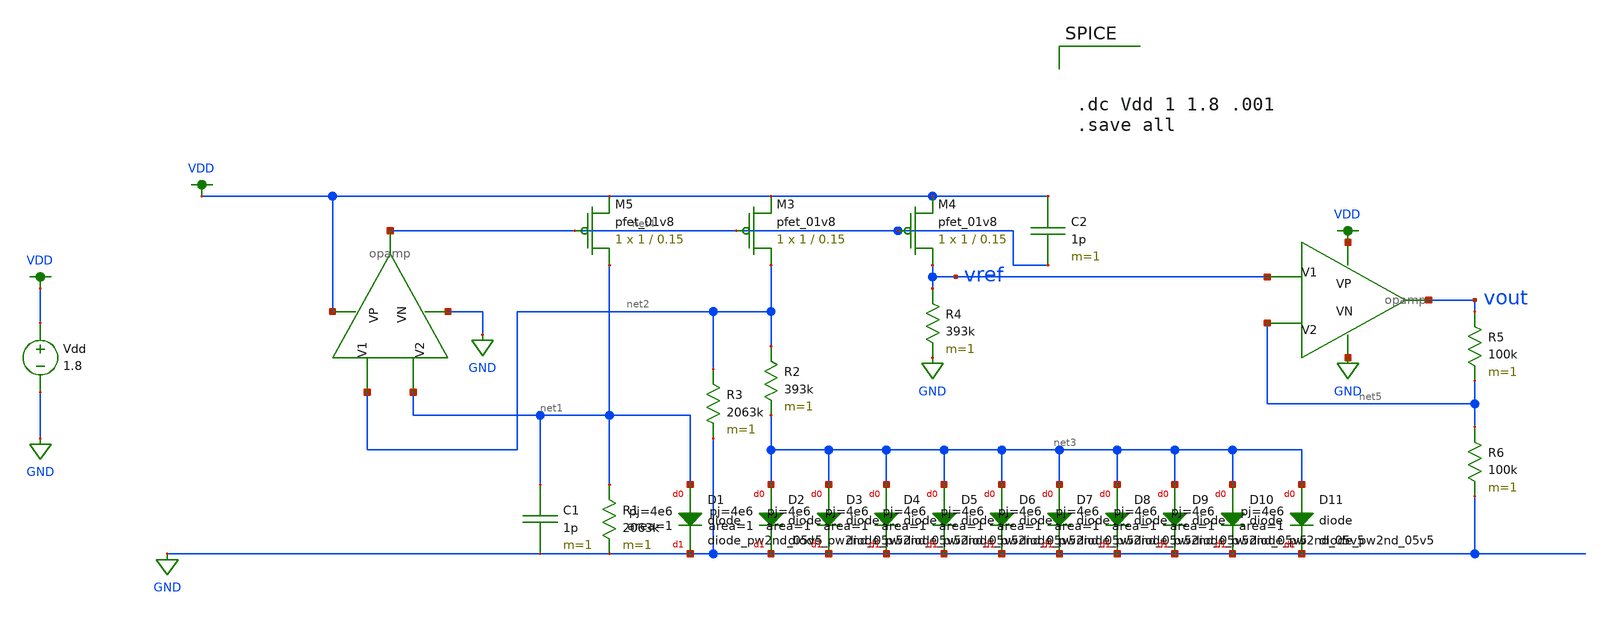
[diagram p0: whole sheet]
** sch_path: schematics/bandgap.sch
**.subckt bandgap
XD1 net1 GND sky130_fd_pr__diode_pw2nd_05v5 area=1 pj=4e6
XM4 vref net4 VDD VDD sky130_fd_pr__pfet_01v8 L=0.15 W=1 nf=1 ad='int((nf+1)/2) * W/nf * 0.29' as='int((nf+2)/2) * W/nf * 0.29'
+ pd='2*int((nf+1)/2) * (W/nf + 0.29)' ps='2*int((nf+2)/2) * (W/nf + 0.29)' nrd='0.29 / W' nrs='0.29 / W'
+ sa=0 sb=0 sd=0 mult=1 m=1
XM5 net1 net4 VDD VDD sky130_fd_pr__pfet_01v8 L=0.15 W=1 nf=1 ad='int((nf+1)/2) * W/nf * 0.29' as='int((nf+2)/2) * W/nf * 0.29'
+ pd='2*int((nf+1)/2) * (W/nf + 0.29)' ps='2*int((nf+2)/2) * (W/nf + 0.29)' nrd='0.29 / W' nrs='0.29 / W'
+ sa=0 sb=0 sd=0 mult=1 m=1
XM3 net2 net4 VDD VDD sky130_fd_pr__pfet_01v8 L=0.15 W=1 nf=1 ad='int((nf+1)/2) * W/nf * 0.29' as='int((nf+2)/2) * W/nf * 0.29'
+ pd='2*int((nf+1)/2) * (W/nf + 0.29)' ps='2*int((nf+2)/2) * (W/nf + 0.29)' nrd='0.29 / W' nrs='0.29 / W'
+ sa=0 sb=0 sd=0 mult=1 m=1
C1 net1 GND 1p m=1
R1 net1 GND 2063k m=1
XD2 net3 GND sky130_fd_pr__diode_pw2nd_05v5 area=1 pj=4e6
R2 net2 net3 393k m=1
XD3 net3 GND sky130_fd_pr__diode_pw2nd_05v5 area=1 pj=4e6
R3 net2 GND 2063k m=1
R4 vref GND 393k m=1
XD4 net3 GND sky130_fd_pr__diode_pw2nd_05v5 area=1 pj=4e6
XD5 net3 GND sky130_fd_pr__diode_pw2nd_05v5 area=1 pj=4e6
XD6 net3 GND sky130_fd_pr__diode_pw2nd_05v5 area=1 pj=4e6
XD7 net3 GND sky130_fd_pr__diode_pw2nd_05v5 area=1 pj=4e6
XD8 net3 GND sky130_fd_pr__diode_pw2nd_05v5 area=1 pj=4e6
XD9 net3 GND sky130_fd_pr__diode_pw2nd_05v5 area=1 pj=4e6
XD10 net3 GND sky130_fd_pr__diode_pw2nd_05v5 area=1 pj=4e6
XD11 net3 GND sky130_fd_pr__diode_pw2nd_05v5 area=1 pj=4e6
C2 VDD net4 1p m=1
Vdd VDD GND 1.8
X1 net2 net1 VDD GND net4 opamp
X2 vref net5 VDD GND vout opamp
R5 vout net5 100k m=1
R6 net5 GND 100k m=1
**** begin user architecture code

.option wnflag=1
.param MC_SWITCH=0.0
.lib ~/skywater/skywater-pdk/libraries/sky130_fd_pr_ngspice/latest/models/sky130.lib.spice tt




.dc Vdd 1 1.8 .001
.save all


**** end user architecture code
**.ends

* expanding   symbol:  /home/madvlsi/Documents/MADVLSI_final/schematics/opamp.sym # of pins=5
** sym_path: schematics/opamp.sym
** sch_path: schematics/opamp.sch
.subckt opamp V1 V2 VP VN Vout
*.ipin V1
*.ipin V2
*.opin Vout
*.iopin VP
*.iopin VN
*.iopin VP
*.iopin VN
XM1 VN net7 net2 GND sky130_fd_pr__nfet_01v8 L=l W=w nf=1 ad='int((nf+1)/2) * W/nf * 0.29' as='int((nf+2)/2) * W/nf * 0.29'
+ pd='2*int((nf+1)/2) * (W/nf + 0.29)' ps='2*int((nf+2)/2) * (W/nf + 0.29)' nrd='0.29 / W' nrs='0.29 / W'
+ sa=0 sb=0 sd=0 mult=1 m=1
XM2 VP net3 net1 VDD sky130_fd_pr__pfet_01v8 L=l W=w nf=1 ad='int((nf+1)/2) * W/nf * 0.29' as='int((nf+2)/2) * W/nf * 0.29'
+ pd='2*int((nf+1)/2) * (W/nf + 0.29)' ps='2*int((nf+2)/2) * (W/nf + 0.29)' nrd='0.29 / W' nrs='0.29 / W'
+ sa=0 sb=0 sd=0 mult=1 m=1
XM3 net1 V1 Vd VDD sky130_fd_pr__pfet_01v8 L=l W=w nf=1 ad='int((nf+1)/2) * W/nf * 0.29' as='int((nf+2)/2) * W/nf * 0.29'
+ pd='2*int((nf+1)/2) * (W/nf + 0.29)' ps='2*int((nf+2)/2) * (W/nf + 0.29)' nrd='0.29 / W' nrs='0.29 / W'
+ sa=0 sb=0 sd=0 mult=1 m=1
XM4 Vc V2 net1 VDD sky130_fd_pr__pfet_01v8 L=l W=w nf=1 ad='int((nf+1)/2) * W/nf * 0.29' as='int((nf+2)/2) * W/nf * 0.29'
+ pd='2*int((nf+1)/2) * (W/nf + 0.29)' ps='2*int((nf+2)/2) * (W/nf + 0.29)' nrd='0.29 / W' nrs='0.29 / W'
+ sa=0 sb=0 sd=0 mult=1 m=1
XM5 Va V2 net2 GND sky130_fd_pr__nfet_01v8 L=l W=w nf=1 ad='int((nf+1)/2) * W/nf * 0.29' as='int((nf+2)/2) * W/nf * 0.29'
+ pd='2*int((nf+1)/2) * (W/nf + 0.29)' ps='2*int((nf+2)/2) * (W/nf + 0.29)' nrd='0.29 / W' nrs='0.29 / W'
+ sa=0 sb=0 sd=0 mult=1 m=1
XM6 net2 V1 Vb GND sky130_fd_pr__nfet_01v8 L=l W=w nf=1 ad='int((nf+1)/2) * W/nf * 0.29' as='int((nf+2)/2) * W/nf * 0.29'
+ pd='2*int((nf+1)/2) * (W/nf + 0.29)' ps='2*int((nf+2)/2) * (W/nf + 0.29)' nrd='0.29 / W' nrs='0.29 / W'
+ sa=0 sb=0 sd=0 mult=1 m=1
XM7 net3 net3 Va VDD sky130_fd_pr__pfet_01v8 L=l W=w nf=1 ad='int((nf+1)/2) * W/nf * 0.29' as='int((nf+2)/2) * W/nf * 0.29'
+ pd='2*int((nf+1)/2) * (W/nf + 0.29)' ps='2*int((nf+2)/2) * (W/nf + 0.29)' nrd='0.29 / W' nrs='0.29 / W'
+ sa=0 sb=0 sd=0 mult=1 m=1
XM8 net6 net6 Va VDD sky130_fd_pr__pfet_01v8 L=l W=w nf=1 ad='int((nf+1)/2) * W/nf * 0.29' as='int((nf+2)/2) * W/nf * 0.29'
+ pd='2*int((nf+1)/2) * (W/nf + 0.29)' ps='2*int((nf+2)/2) * (W/nf + 0.29)' nrd='0.29 / W' nrs='0.29 / W'
+ sa=0 sb=0 sd=0 mult=1 m=1
XM9 net5 net6 Vb VDD sky130_fd_pr__pfet_01v8 L=l W=w nf=1 ad='int((nf+1)/2) * W/nf * 0.29' as='int((nf+2)/2) * W/nf * 0.29'
+ pd='2*int((nf+1)/2) * (W/nf + 0.29)' ps='2*int((nf+2)/2) * (W/nf + 0.29)' nrd='0.29 / W' nrs='0.29 / W'
+ sa=0 sb=0 sd=0 mult=1 m=1
XM10 Va net3 VP VDD sky130_fd_pr__pfet_01v8 L=l W=w nf=1 ad='int((nf+1)/2) * W/nf * 0.29' as='int((nf+2)/2) * W/nf * 0.29'
+ pd='2*int((nf+1)/2) * (W/nf + 0.29)' ps='2*int((nf+2)/2) * (W/nf + 0.29)' nrd='0.29 / W' nrs='0.29 / W'
+ sa=0 sb=0 sd=0 mult=1 m=1
XM11 Vb net3 VP VDD sky130_fd_pr__pfet_01v8 L=l W=w nf=1 ad='int((nf+1)/2) * W/nf * 0.29' as='int((nf+2)/2) * W/nf * 0.29'
+ pd='2*int((nf+1)/2) * (W/nf + 0.29)' ps='2*int((nf+2)/2) * (W/nf + 0.29)' nrd='0.29 / W' nrs='0.29 / W'
+ sa=0 sb=0 sd=0 mult=1 m=1
XM12 net6 net6 Vc GND sky130_fd_pr__nfet_01v8 L=l W=w nf=1 ad='int((nf+1)/2) * W/nf * 0.29' as='int((nf+2)/2) * W/nf * 0.29'
+ pd='2*int((nf+1)/2) * (W/nf + 0.29)' ps='2*int((nf+2)/2) * (W/nf + 0.29)' nrd='0.29 / W' nrs='0.29 / W'
+ sa=0 sb=0 sd=0 mult=1 m=1
XM13 net5 net6 Vd GND sky130_fd_pr__nfet_01v8 L=l W=w nf=1 ad='int((nf+1)/2) * W/nf * 0.29' as='int((nf+2)/2) * W/nf * 0.29'
+ pd='2*int((nf+1)/2) * (W/nf + 0.29)' ps='2*int((nf+2)/2) * (W/nf + 0.29)' nrd='0.29 / W' nrs='0.29 / W'
+ sa=0 sb=0 sd=0 mult=1 m=1
XM14 Vc net7 VN GND sky130_fd_pr__nfet_01v8 L=l W=w nf=1 ad='int((nf+1)/2) * W/nf * 0.29' as='int((nf+2)/2) * W/nf * 0.29'
+ pd='2*int((nf+1)/2) * (W/nf + 0.29)' ps='2*int((nf+2)/2) * (W/nf + 0.29)' nrd='0.29 / W' nrs='0.29 / W'
+ sa=0 sb=0 sd=0 mult=1 m=1
XM15 Vd net7 VN GND sky130_fd_pr__nfet_01v8 L=l W=w nf=1 ad='int((nf+1)/2) * W/nf * 0.29' as='int((nf+2)/2) * W/nf * 0.29'
+ pd='2*int((nf+1)/2) * (W/nf + 0.29)' ps='2*int((nf+2)/2) * (W/nf + 0.29)' nrd='0.29 / W' nrs='0.29 / W'
+ sa=0 sb=0 sd=0 mult=1 m=1
XM16 net8 net7 net3 GND sky130_fd_pr__nfet_01v8 L=l W=w nf=1 ad='int((nf+1)/2) * W/nf * 0.29' as='int((nf+2)/2) * W/nf * 0.29'
+ pd='2*int((nf+1)/2) * (W/nf + 0.29)' ps='2*int((nf+2)/2) * (W/nf + 0.29)' nrd='0.29 / W' nrs='0.29 / W'
+ sa=0 sb=0 sd=0 mult=1 m=1
XM17 VN net7 net8 GND sky130_fd_pr__nfet_01v8 L=l W=w nf=1 ad='int((nf+1)/2) * W/nf * 0.29' as='int((nf+2)/2) * W/nf * 0.29'
+ pd='2*int((nf+1)/2) * (W/nf + 0.29)' ps='2*int((nf+2)/2) * (W/nf + 0.29)' nrd='0.29 / W' nrs='0.29 / W'
+ sa=0 sb=0 sd=0 mult=1 m=1
XM18 net8 net7 VP GND sky130_fd_pr__nfet_01v8 L=l W=w nf=1 ad='int((nf+1)/2) * W/nf * 0.29' as='int((nf+2)/2) * W/nf * 0.29'
+ pd='2*int((nf+1)/2) * (W/nf + 0.29)' ps='2*int((nf+2)/2) * (W/nf + 0.29)' nrd='0.29 / W' nrs='0.29 / W'
+ sa=0 sb=0 sd=0 mult=M m=M
XM19 net4 net3 net7 VDD sky130_fd_pr__pfet_01v8 L=l W=w nf=1 ad='int((nf+1)/2) * W/nf * 0.29' as='int((nf+2)/2) * W/nf * 0.29'
+ pd='2*int((nf+1)/2) * (W/nf + 0.29)' ps='2*int((nf+2)/2) * (W/nf + 0.29)' nrd='0.29 / W' nrs='0.29 / W'
+ sa=0 sb=0 sd=0 mult=1 m=1
XM20 VP net3 net4 VDD sky130_fd_pr__pfet_01v8 L=l W=w nf=1 ad='int((nf+1)/2) * W/nf * 0.29' as='int((nf+2)/2) * W/nf * 0.29'
+ pd='2*int((nf+1)/2) * (W/nf + 0.29)' ps='2*int((nf+2)/2) * (W/nf + 0.29)' nrd='0.29 / W' nrs='0.29 / W'
+ sa=0 sb=0 sd=0 mult=1 m=1
XM21 net4 net3 VN VDD sky130_fd_pr__pfet_01v8 L=l W=w nf=1 ad='int((nf+1)/2) * W/nf * 0.29' as='int((nf+2)/2) * W/nf * 0.29'
+ pd='2*int((nf+1)/2) * (W/nf + 0.29)' ps='2*int((nf+2)/2) * (W/nf + 0.29)' nrd='0.29 / W' nrs='0.29 / W'
+ sa=0 sb=0 sd=0 mult=M m=M
XM22 net7 net7 Vc GND sky130_fd_pr__nfet_01v8 L=l W=w nf=1 ad='int((nf+1)/2) * W/nf * 0.29' as='int((nf+2)/2) * W/nf * 0.29'
+ pd='2*int((nf+1)/2) * (W/nf + 0.29)' ps='2*int((nf+2)/2) * (W/nf + 0.29)' nrd='0.29 / W' nrs='0.29 / W'
+ sa=0 sb=0 sd=0 mult=1 m=1
**** begin user architecture code

.param M=3
.param w=3
.param l=0.6


**** end user architecture code
XM23 Vout net5 VN GND sky130_fd_pr__nfet_01v8 L=.15 W=6 nf=1 ad='int((nf+1)/2) * W/nf * 0.29' as='int((nf+2)/2) * W/nf * 0.29'
+ pd='2*int((nf+1)/2) * (W/nf + 0.29)' ps='2*int((nf+2)/2) * (W/nf + 0.29)' nrd='0.29 / W' nrs='0.29 / W'
+ sa=0 sb=0 sd=0 mult=1 m=1
XM24 Vout net5 VP VDD sky130_fd_pr__pfet_01v8 L=.15 W=12 nf=1 ad='int((nf+1)/2) * W/nf * 0.29' as='int((nf+2)/2) * W/nf * 0.29'
+ pd='2*int((nf+1)/2) * (W/nf + 0.29)' ps='2*int((nf+2)/2) * (W/nf + 0.29)' nrd='0.29 / W' nrs='0.29 / W'
+ sa=0 sb=0 sd=0 mult=1 m=1
C1 Vout net5 500f m=1
.ends

.GLOBAL VDD
.GLOBAL GND
.end
